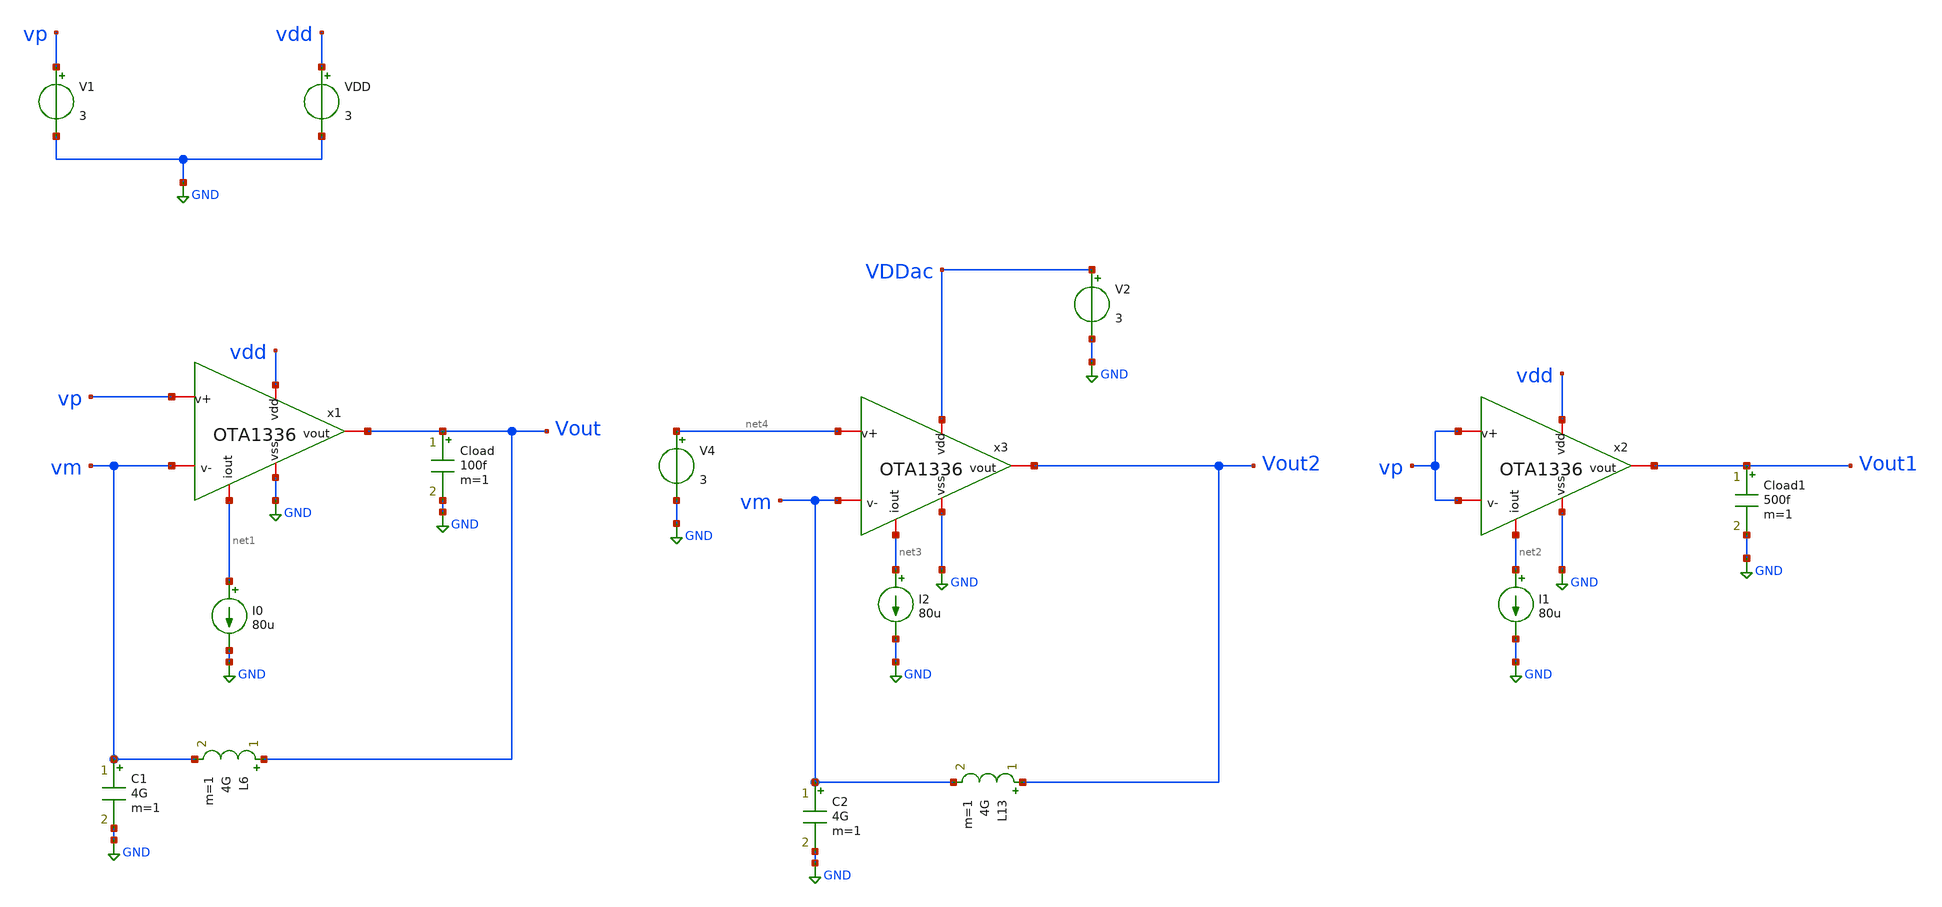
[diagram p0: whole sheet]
** sch_path: tests/data/OTA1336/testbenches/ac/xschem/payload/OTA1336_pex_tb.sch
**.subckt OTA1336_pex_tb
V1 vp GND 3
VDD vdd GND 3
I0 net1 GND 80u
Cload Vout GND 100f m=1
L6 Vout vm 4G m=1
C1 vm GND 4G m=1
I1 net2 GND 80u
Cload1 Vout1 GND 500f m=1
I2 net3 GND 80u
L13 Vout2 vm 4G m=1
C2 vm GND 4G m=1
V2 VDDac GND 3
V4 net4 GND 3
x1 vdd net1 Vout vm vp GND OTA1336
x3 VDDac net3 Vout2 vm net4 GND OTA1336
x2 vdd net2 Vout1 vp vp GND OTA1336
**** begin user architecture code
 value=

blabla

**** end user architecture code
**.ends
.GLOBAL GND
.end
